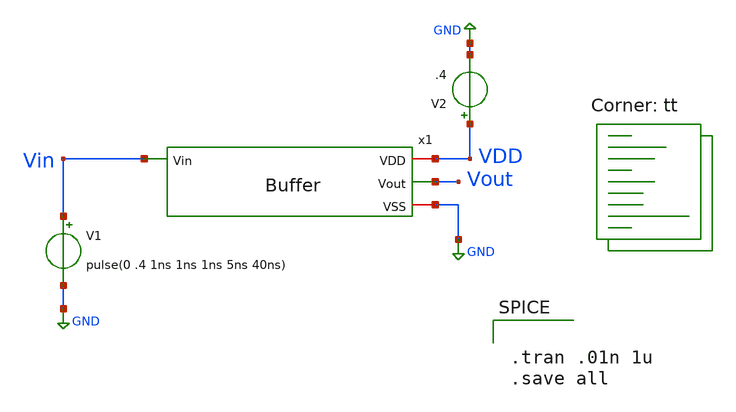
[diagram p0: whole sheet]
** sch_path: xschem/Testbenches/BufferTB.sch
**.subckt BufferTB
x1 VDD Vin Vout GND Buffer
V1 Vin GND pulse(0 .4 1ns 1ns 1ns 5ns 40ns)
V2 VDD GND .4
**** begin user architecture code
.lib $::SKYWATER_MODELS/sky130.lib.spice tt


.tran .01n 1u
.save all

**** end user architecture code
**.ends

* expanding   symbol:  Buffer.sym # of pins=4
** sym_path: xschem/Buffer.sym
** sch_path: xschem/Buffer.sch
.subckt Buffer VDD Vin Vout VSS
*.iopin VDD
*.iopin VSS
*.ipin Vin
*.opin Vout
x1 VDD Vin net1 VSS Inverter
x2 VDD net1 Vout VSS Inverter
.ends


* expanding   symbol:  Inverter.sym # of pins=4
** sym_path: xschem/Inverter.sym
** sch_path: xschem/Inverter.sch
.subckt Inverter VDD Vin Vout VSS
*.ipin Vin
*.iopin VDD
*.iopin VSS
*.opin Vout
XM1 Vout Vin VSS VSS sky130_fd_pr__nfet_g5v0d10v5 L=0.5 W=0.75 nf=1 ad='int((nf+1)/2) * W/nf * 0.29'
+ as='int((nf+2)/2) * W/nf * 0.29' pd='2*int((nf+1)/2) * (W/nf + 0.29)' ps='2*int((nf+2)/2) * (W/nf + 0.29)'
+ nrd='0.29 / W' nrs='0.29 / W' sa=0 sb=0 sd=0 mult=1 m=1
XM2 Vout Vin VDD VDD sky130_fd_pr__pfet_g5v0d10v5 L=0.5 W=1.5 nf=1 ad='int((nf+1)/2) * W/nf * 0.29' as='int((nf+2)/2) * W/nf * 0.29'
+ pd='2*int((nf+1)/2) * (W/nf + 0.29)' ps='2*int((nf+2)/2) * (W/nf + 0.29)' nrd='0.29 / W' nrs='0.29 / W'
+ sa=0 sb=0 sd=0 mult=1 m=1
.ends

.GLOBAL GND
.end
